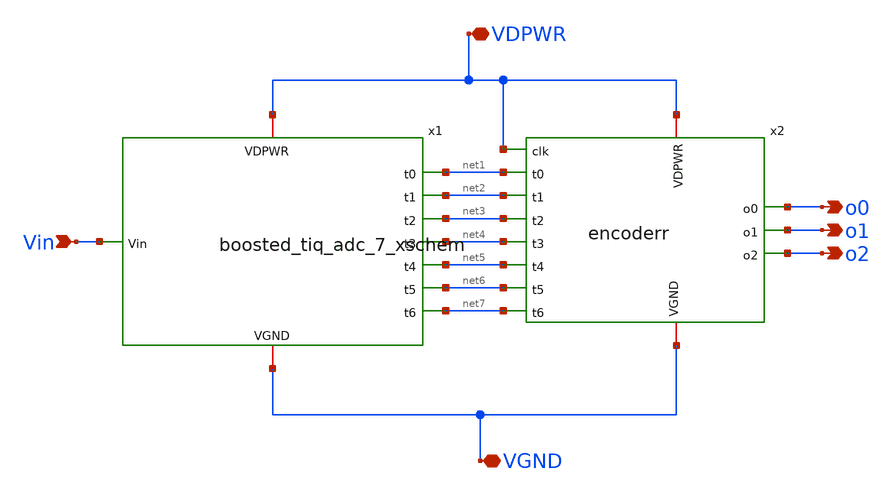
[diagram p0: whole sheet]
** sch_path: tt_um_emmersonv_tiq_adc/xschem/full_tiq_adc_3.sch
**.subckt full_tiq_adc_3 VGND VDPWR Vin o0 o1 o2
*.iopin VGND
*.iopin VDPWR
*.ipin Vin
*.opin o0
*.opin o1
*.opin o2
x1 VDPWR net1 net2 net3 Vin net4 net5 net6 net7 VGND boosted_tiq_adc_7_xschem
x2 VGND VDPWR VDPWR o0 o1 o2 net1 net2 net3 net4 net5 net6 net7 encoderr
**.ends
.end
